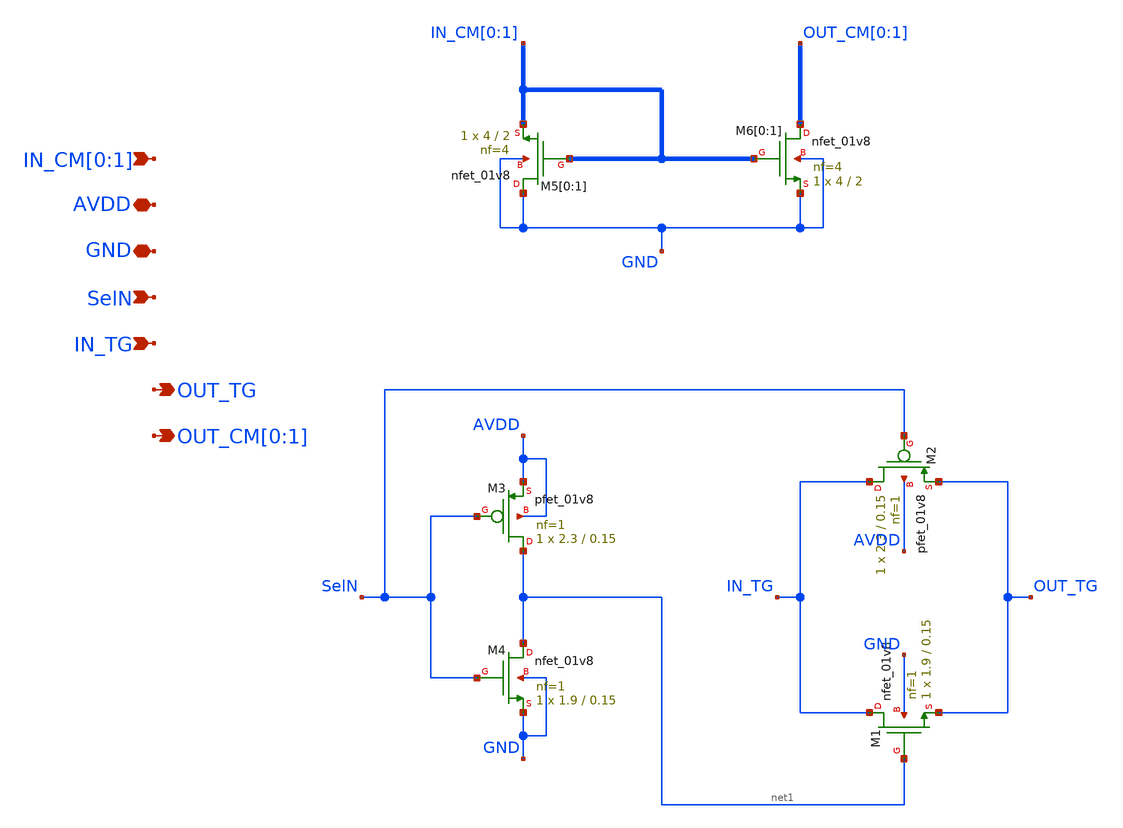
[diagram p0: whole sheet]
** sch_path: sky130_cells/TGate_2nMirror/TGate_2nMirror.sch
**.subckt TGate_2nMirror SelN AVDD IN_TG OUT_TG IN_CM[0],IN_CM[1] OUT_CM[0],OUT_CM[1] GND
*.ipin SelN
*.iopin AVDD
*.ipin IN_TG
*.opin OUT_TG
*.ipin IN_CM[0],IN_CM[1]
*.opin OUT_CM[0],OUT_CM[1]
*.iopin GND
XM1 IN_TG net1 OUT_TG GND sky130_fd_pr__nfet_01v8 L=0.15 W=1.9 nf=1 ad='int((1 + 1)/2) * 1.9 / 1 * 0.29'
+ as='int((1 + 2)/2) * 1.9 / 1 * 0.29' pd='2*int((1 + 1)/2) * (1.9 / 1 + 0.29)' ps='2*int((1 + 2)/2) * (1.9 / 1 + 0.29)'
+ nrd='0.29 / 1.9 ' nrs='0.29 / 1.9 ' sa=0 sb=0 sd=0 mult=1 m=1
XM2 IN_TG SelN OUT_TG AVDD sky130_fd_pr__pfet_01v8 L=0.15 W=2.3 nf=1 ad='int((1 + 1)/2) * 2.3 / 1 * 0.29'
+ as='int((1 + 2)/2) * 2.3 / 1 * 0.29' pd='2*int((1 + 1)/2) * (2.3 / 1 + 0.29)' ps='2*int((1 + 2)/2) * (2.3 / 1 + 0.29)'
+ nrd='0.29 / 2.3 ' nrs='0.29 / 2.3 ' sa=0 sb=0 sd=0 mult=1 m=1
XM3 net1 SelN AVDD AVDD sky130_fd_pr__pfet_01v8 L=0.15 W=2.3 nf=1 ad='int((1 + 1)/2) * 2.3 / 1 * 0.29'
+ as='int((1 + 2)/2) * 2.3 / 1 * 0.29' pd='2*int((1 + 1)/2) * (2.3 / 1 + 0.29)' ps='2*int((1 + 2)/2) * (2.3 / 1 + 0.29)'
+ nrd='0.29 / 2.3 ' nrs='0.29 / 2.3 ' sa=0 sb=0 sd=0 mult=1 m=1
XM4 net1 SelN GND GND sky130_fd_pr__nfet_01v8 L=0.15 W=1.9 nf=1 ad='int((1 + 1)/2) * 1.9 / 1 * 0.29'
+ as='int((1 + 2)/2) * 1.9 / 1 * 0.29' pd='2*int((1 + 1)/2) * (1.9 / 1 + 0.29)' ps='2*int((1 + 2)/2) * (1.9 / 1 + 0.29)'
+ nrd='0.29 / 1.9 ' nrs='0.29 / 1.9 ' sa=0 sb=0 sd=0 mult=1 m=1
XM5[0] GND IN_CM[0] IN_CM[0] GND sky130_fd_pr__nfet_01v8 L=2 W=4 nf=4 ad='int((4 + 1)/2) * 4 / 4 * 0.29'
+ as='int((4 + 2)/2) * 4 / 4 * 0.29' pd='2*int((4 + 1)/2) * (4 / 4 + 0.29)' ps='2*int((4 + 2)/2) * (4 / 4 + 0.29)'
+ nrd='0.29 / 4 ' nrs='0.29 / 4 ' sa=0 sb=0 sd=0 mult=1 m=1
XM5[1] GND IN_CM[1] IN_CM[1] GND sky130_fd_pr__nfet_01v8 L=2 W=4 nf=4 ad='int((4 + 1)/2) * 4 / 4 * 0.29'
+ as='int((4 + 2)/2) * 4 / 4 * 0.29' pd='2*int((4 + 1)/2) * (4 / 4 + 0.29)' ps='2*int((4 + 2)/2) * (4 / 4 + 0.29)'
+ nrd='0.29 / 4 ' nrs='0.29 / 4 ' sa=0 sb=0 sd=0 mult=1 m=1
XM6[0] OUT_CM[0] IN_CM[0] GND GND sky130_fd_pr__nfet_01v8 L=2 W=4 nf=4 ad='int((4 + 1)/2) * 4 / 4 * 0.29'
+ as='int((4 + 2)/2) * 4 / 4 * 0.29' pd='2*int((4 + 1)/2) * (4 / 4 + 0.29)' ps='2*int((4 + 2)/2) * (4 / 4 + 0.29)'
+ nrd='0.29 / 4 ' nrs='0.29 / 4 ' sa=0 sb=0 sd=0 mult=1 m=1
XM6[1] OUT_CM[1] IN_CM[1] GND GND sky130_fd_pr__nfet_01v8 L=2 W=4 nf=4 ad='int((4 + 1)/2) * 4 / 4 * 0.29'
+ as='int((4 + 2)/2) * 4 / 4 * 0.29' pd='2*int((4 + 1)/2) * (4 / 4 + 0.29)' ps='2*int((4 + 2)/2) * (4 / 4 + 0.29)'
+ nrd='0.29 / 4 ' nrs='0.29 / 4 ' sa=0 sb=0 sd=0 mult=1 m=1
**.ends
.end
